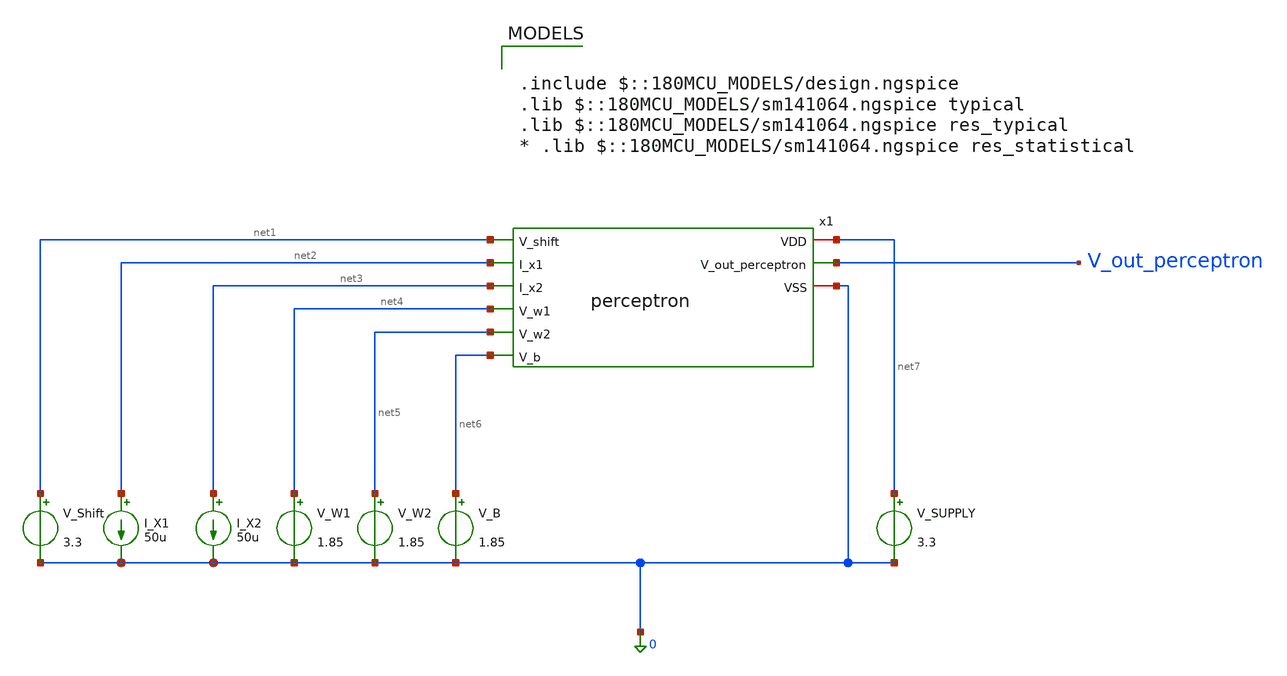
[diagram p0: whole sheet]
** sch_path: schematics/tb_demo_perceptron.sch
**.subckt tb_demo_perceptron
V_SUPPLY net7 0 3.3
I_X1 net2 0 50u
I_X2 net3 0 50u
V_W1 net4 0 1.85
V_W2 net5 0 1.85
V_B net6 0 1.85
V_Shift net1 0 3.3
x1 net7 net1 net2 net3 V_out_perceptron net4 net5 0 net6 perceptron
**** begin user architecture code


.control
  op
  print all
  print v(V_out_perceptron)
.endc



.include $::180MCU_MODELS/design.ngspice
.lib $::180MCU_MODELS/sm141064.ngspice typical
.lib $::180MCU_MODELS/sm141064.ngspice res_typical
* .lib $::180MCU_MODELS/sm141064.ngspice res_statistical

**** end user architecture code
**.ends
.end
